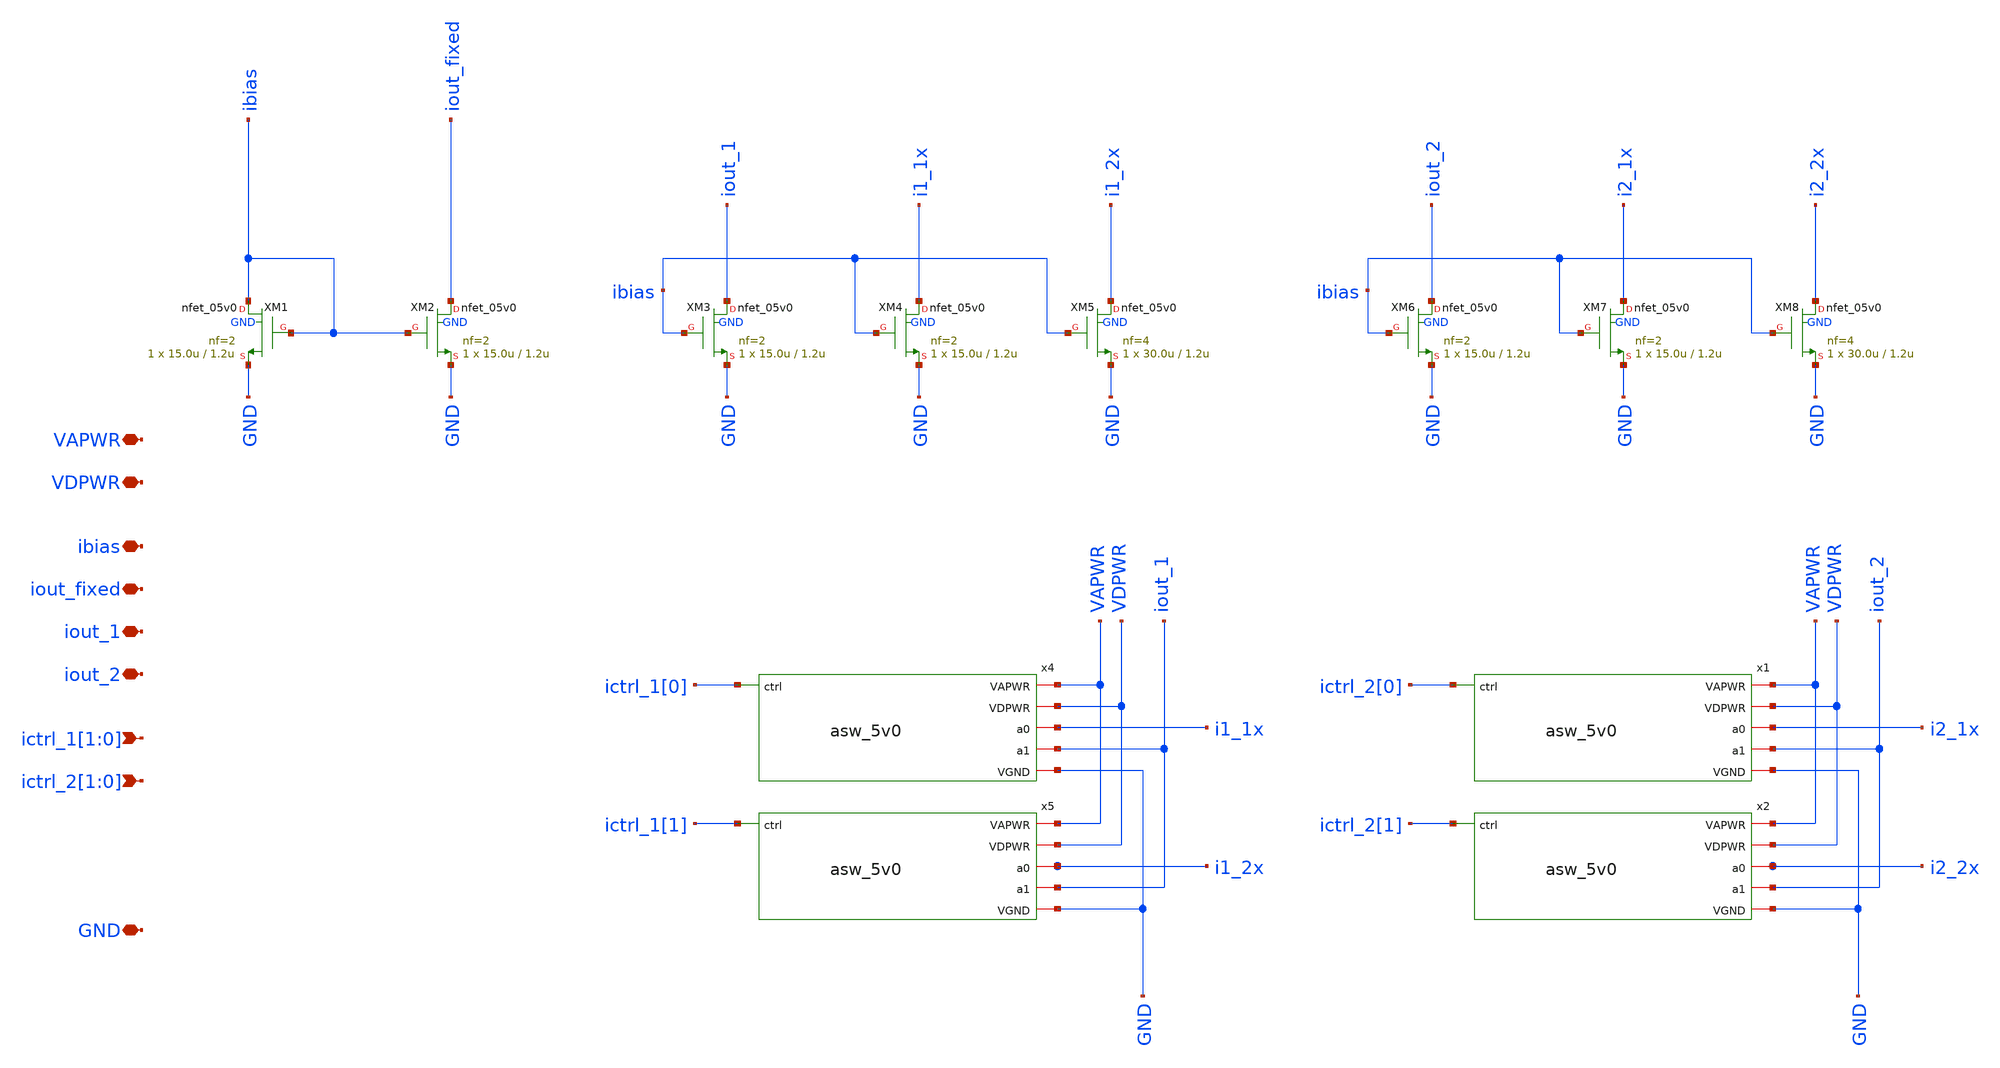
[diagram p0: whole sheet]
** sch_path: xschem/mirror_n.sch
**.subckt mirror_n ibias iout_fixed iout_1 ictrl_1[1],ictrl_1[0] ictrl_2[1],ictrl_2[0] iout_2 VAPWR
*+ VDPWR GND
*.iopin ibias
*.iopin iout_fixed
*.iopin iout_1
*.ipin ictrl_1[1],ictrl_1[0]
*.ipin ictrl_2[1],ictrl_2[0]
*.iopin iout_2
*.iopin VAPWR
*.iopin VDPWR
*.iopin GND
x4 GND VDPWR VAPWR ictrl_1[0] i1_1x iout_1 asw_5v0
x5 GND VDPWR VAPWR ictrl_1[1] i1_2x iout_1 asw_5v0
x1 GND VDPWR VAPWR ictrl_2[0] i2_1x iout_2 asw_5v0
x2 GND VDPWR VAPWR ictrl_2[1] i2_2x iout_2 asw_5v0
XM1 ibias ibias GND GND nfet_05v0 L=1.2u W=15.0u nf=2 ad='int((nf+1)/2) * W/nf * 0.18u' as='int((nf+2)/2) * W/nf * 0.18u'
+ pd='2*int((nf+1)/2) * (W/nf + 0.18u)' ps='2*int((nf+2)/2) * (W/nf + 0.18u)' nrd='0.18u / W' nrs='0.18u / W'
+ sa=0 sb=0 sd=0 m=1 par=1
XM2 iout_fixed ibias GND GND nfet_05v0 L=1.2u W=15.0u nf=2 ad='int((nf+1)/2) * W/nf * 0.18u' as='int((nf+2)/2) * W/nf * 0.18u'
+ pd='2*int((nf+1)/2) * (W/nf + 0.18u)' ps='2*int((nf+2)/2) * (W/nf + 0.18u)' nrd='0.18u / W' nrs='0.18u / W'
+ sa=0 sb=0 sd=0 m=1 par=1
XM3 iout_1 ibias GND GND nfet_05v0 L=1.2u W=15.0u nf=2 ad='int((nf+1)/2) * W/nf * 0.18u' as='int((nf+2)/2) * W/nf * 0.18u'
+ pd='2*int((nf+1)/2) * (W/nf + 0.18u)' ps='2*int((nf+2)/2) * (W/nf + 0.18u)' nrd='0.18u / W' nrs='0.18u / W'
+ sa=0 sb=0 sd=0 m=1 par=1
XM4 i1_1x ibias GND GND nfet_05v0 L=1.2u W=15.0u nf=2 ad='int((nf+1)/2) * W/nf * 0.18u' as='int((nf+2)/2) * W/nf * 0.18u'
+ pd='2*int((nf+1)/2) * (W/nf + 0.18u)' ps='2*int((nf+2)/2) * (W/nf + 0.18u)' nrd='0.18u / W' nrs='0.18u / W'
+ sa=0 sb=0 sd=0 m=1 par=1
XM5 i1_2x ibias GND GND nfet_05v0 L=1.2u W=30.0u nf=4 ad='int((nf+1)/2) * W/nf * 0.18u' as='int((nf+2)/2) * W/nf * 0.18u'
+ pd='2*int((nf+1)/2) * (W/nf + 0.18u)' ps='2*int((nf+2)/2) * (W/nf + 0.18u)' nrd='0.18u / W' nrs='0.18u / W'
+ sa=0 sb=0 sd=0 m=1 par=1
XM6 iout_2 ibias GND GND nfet_05v0 L=1.2u W=15.0u nf=2 ad='int((nf+1)/2) * W/nf * 0.18u' as='int((nf+2)/2) * W/nf * 0.18u'
+ pd='2*int((nf+1)/2) * (W/nf + 0.18u)' ps='2*int((nf+2)/2) * (W/nf + 0.18u)' nrd='0.18u / W' nrs='0.18u / W'
+ sa=0 sb=0 sd=0 m=1 par=1
XM7 i2_1x ibias GND GND nfet_05v0 L=1.2u W=15.0u nf=2 ad='int((nf+1)/2) * W/nf * 0.18u' as='int((nf+2)/2) * W/nf * 0.18u'
+ pd='2*int((nf+1)/2) * (W/nf + 0.18u)' ps='2*int((nf+2)/2) * (W/nf + 0.18u)' nrd='0.18u / W' nrs='0.18u / W'
+ sa=0 sb=0 sd=0 m=1 par=1
XM8 i2_2x ibias GND GND nfet_05v0 L=1.2u W=30.0u nf=4 ad='int((nf+1)/2) * W/nf * 0.18u' as='int((nf+2)/2) * W/nf * 0.18u'
+ pd='2*int((nf+1)/2) * (W/nf + 0.18u)' ps='2*int((nf+2)/2) * (W/nf + 0.18u)' nrd='0.18u / W' nrs='0.18u / W'
+ sa=0 sb=0 sd=0 m=1 par=1
**.ends

* expanding   symbol:  asw_5v0.sym # of pins=6
** sym_path: xschem/asw_5v0.sym
** sch_path: xschem/asw_5v0.sch
.subckt asw_5v0 VGND VDPWR VAPWR ctrl a0 a1
*.ipin ctrl
*.iopin VDPWR
*.iopin VGND
*.iopin a0
*.iopin VAPWR
*.iopin a1
x1 VGND VDPWR VAPWR ctrl tgon_p tgon_n lv2hv
XM1 a0 tgon_n a1 VAPWR pfet_05v0 L=0.50u W=592u nf=16 ad='int((nf+1)/2) * W/nf * 0.18u' as='int((nf+2)/2) * W/nf * 0.18u'
+ pd='2*int((nf+1)/2) * (W/nf + 0.18u)' ps='2*int((nf+2)/2) * (W/nf + 0.18u)' nrd='0.18u / W' nrs='0.18u / W'
+ sa=0 sb=0 sd=0 m=1 par=1
XM2 a1 tgon_p a0 VGND nfet_05v0 L=0.60u W=248u nf=8 ad='int((nf+1)/2) * W/nf * 0.18u' as='int((nf+2)/2) * W/nf * 0.18u'
+ pd='2*int((nf+1)/2) * (W/nf + 0.18u)' ps='2*int((nf+2)/2) * (W/nf + 0.18u)' nrd='0.18u / W' nrs='0.18u / W'
+ sa=0 sb=0 sd=0 m=1 par=1
.ends


* expanding   symbol:  lv2hv.sym # of pins=6
** sym_path: lv2hv.sym
** sch_path: lv2hv.sch
.subckt lv2hv VGND VDPWR VAPWR in out_p out_n
*.iopin VAPWR
*.iopin VGND
*.ipin in
*.iopin VDPWR
*.opin out_p
*.opin out_n
XM1 in_n in VGND VGND nfet_03v3 L=0.28u W=0.89u nf=1 ad='int((nf+1)/2) * W/nf * 0.18u' as='int((nf+2)/2) * W/nf * 0.18u'
+ pd='2*int((nf+1)/2) * (W/nf + 0.18u)' ps='2*int((nf+2)/2) * (W/nf + 0.18u)' nrd='0.18u / W' nrs='0.18u / W'
+ sa=0 sb=0 sd=0 m=1 par=1
XM2 in_n in VDPWR VDPWR pfet_03v3 L=0.28u W=2.0u nf=1 ad='int((nf+1)/2) * W/nf * 0.18u' as='int((nf+2)/2) * W/nf * 0.18u'
+ pd='2*int((nf+1)/2) * (W/nf + 0.18u)' ps='2*int((nf+2)/2) * (W/nf + 0.18u)' nrd='0.18u / W' nrs='0.18u / W'
+ sa=0 sb=0 sd=0 m=1 par=1
XM3 VGND in_p net1 VGND nfet_05v0 L=0.6u W=0.5u nf=1 ad='int((nf+1)/2) * W/nf * 0.18u' as='int((nf+2)/2) * W/nf * 0.18u'
+ pd='2*int((nf+1)/2) * (W/nf + 0.18u)' ps='2*int((nf+2)/2) * (W/nf + 0.18u)' nrd='0.18u / W' nrs='0.18u / W'
+ sa=0 sb=0 sd=0 m=1 par=1
XM4 net1 net2 VAPWR VAPWR pfet_05v0 L=0.5u W=0.5u nf=1 ad='int((nf+1)/2) * W/nf * 0.18u' as='int((nf+2)/2) * W/nf * 0.18u'
+ pd='2*int((nf+1)/2) * (W/nf + 0.18u)' ps='2*int((nf+2)/2) * (W/nf + 0.18u)' nrd='0.18u / W' nrs='0.18u / W'
+ sa=0 sb=0 sd=0 m=1 par=1
XM5 net2 in_n VGND VGND nfet_05v0 L=0.6u W=0.5u nf=1 ad='int((nf+1)/2) * W/nf * 0.18u' as='int((nf+2)/2) * W/nf * 0.18u'
+ pd='2*int((nf+1)/2) * (W/nf + 0.18u)' ps='2*int((nf+2)/2) * (W/nf + 0.18u)' nrd='0.18u / W' nrs='0.18u / W'
+ sa=0 sb=0 sd=0 m=1 par=1
XM6 net2 net1 VAPWR VAPWR pfet_05v0 L=0.5u W=0.5u nf=1 ad='int((nf+1)/2) * W/nf * 0.18u' as='int((nf+2)/2) * W/nf * 0.18u'
+ pd='2*int((nf+1)/2) * (W/nf + 0.18u)' ps='2*int((nf+2)/2) * (W/nf + 0.18u)' nrd='0.18u / W' nrs='0.18u / W'
+ sa=0 sb=0 sd=0 m=1 par=1
XM7 VGND net2 out_n VGND nfet_05v0 L=0.60u W=0.5u nf=1 ad='int((nf+1)/2) * W/nf * 0.18u' as='int((nf+2)/2) * W/nf * 0.18u'
+ pd='2*int((nf+1)/2) * (W/nf + 0.18u)' ps='2*int((nf+2)/2) * (W/nf + 0.18u)' nrd='0.18u / W' nrs='0.18u / W'
+ sa=0 sb=0 sd=0 m=1 par=1
XM8 out_n net2 VAPWR VAPWR pfet_05v0 L=0.5u W=1.0u nf=2 ad='int((nf+1)/2) * W/nf * 0.18u' as='int((nf+2)/2) * W/nf * 0.18u'
+ pd='2*int((nf+1)/2) * (W/nf + 0.18u)' ps='2*int((nf+2)/2) * (W/nf + 0.18u)' nrd='0.18u / W' nrs='0.18u / W'
+ sa=0 sb=0 sd=0 m=1 par=1
XM9 VGND net1 out_p VGND nfet_05v0 L=0.60u W=0.5u nf=1 ad='int((nf+1)/2) * W/nf * 0.18u' as='int((nf+2)/2) * W/nf * 0.18u'
+ pd='2*int((nf+1)/2) * (W/nf + 0.18u)' ps='2*int((nf+2)/2) * (W/nf + 0.18u)' nrd='0.18u / W' nrs='0.18u / W'
+ sa=0 sb=0 sd=0 m=1 par=1
XM10 out_p net1 VAPWR VAPWR pfet_05v0 L=0.5u W=1.0u nf=2 ad='int((nf+1)/2) * W/nf * 0.18u' as='int((nf+2)/2) * W/nf * 0.18u'
+ pd='2*int((nf+1)/2) * (W/nf + 0.18u)' ps='2*int((nf+2)/2) * (W/nf + 0.18u)' nrd='0.18u / W' nrs='0.18u / W'
+ sa=0 sb=0 sd=0 m=1 par=1
XM11 in_p in_n VGND VGND nfet_03v3 L=0.28u W=0.89u nf=1 ad='int((nf+1)/2) * W/nf * 0.18u' as='int((nf+2)/2) * W/nf * 0.18u'
+ pd='2*int((nf+1)/2) * (W/nf + 0.18u)' ps='2*int((nf+2)/2) * (W/nf + 0.18u)' nrd='0.18u / W' nrs='0.18u / W'
+ sa=0 sb=0 sd=0 m=1 par=1
XM12 in_p in_n VDPWR VDPWR pfet_03v3 L=0.28u W=2.0u nf=1 ad='int((nf+1)/2) * W/nf * 0.18u' as='int((nf+2)/2) * W/nf * 0.18u'
+ pd='2*int((nf+1)/2) * (W/nf + 0.18u)' ps='2*int((nf+2)/2) * (W/nf + 0.18u)' nrd='0.18u / W' nrs='0.18u / W'
+ sa=0 sb=0 sd=0 m=1 par=1
.ends

.end
